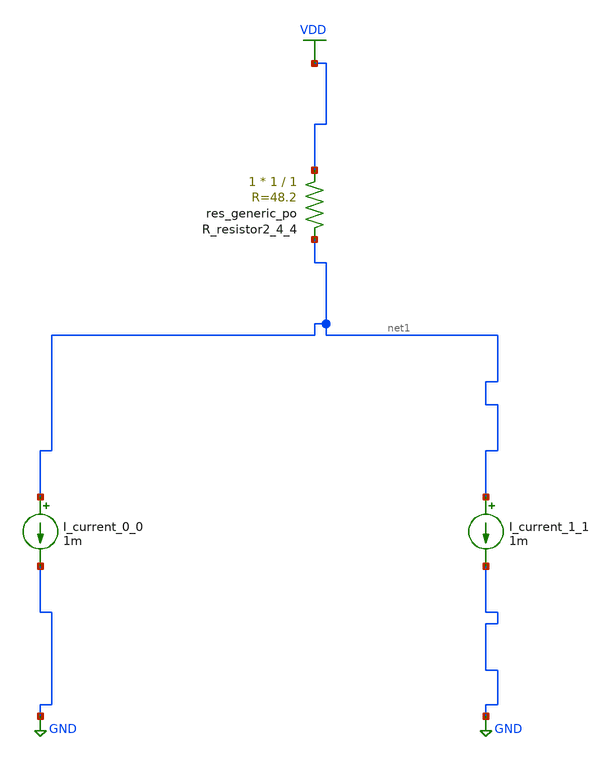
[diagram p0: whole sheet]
** sch_path: schematics/AMSNet/767.sch
**.subckt 767
I_current_0_0 net1 GND 1m
I_current_1_1 net1 GND 1m
XR_resistor2_4_4 VDD net1 sky130_fd_pr__res_generic_po W=1 L=1 m=1
**.ends
.GLOBAL GND
.GLOBAL VDD
.end
